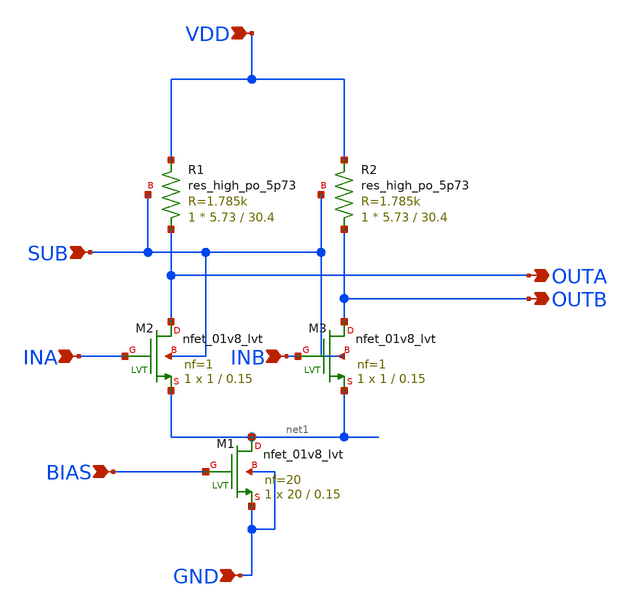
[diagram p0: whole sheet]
** sch_path: hiarachy_final/buffer_amp.sch
**.subckt buffer_amp INA INB BIAS GND VDD SUB OUTA OUTB
*.ipin INA
*.ipin INB
*.ipin BIAS
*.ipin GND
*.ipin VDD
*.ipin SUB
*.opin OUTA
*.opin OUTB
XM1 net1 BIAS GND GND sky130_fd_pr__nfet_01v8_lvt L=0.15 W=20 nf=20 ad='int((nf+1)/2) * W/nf * 0.29'
+ as='int((nf+2)/2) * W/nf * 0.29' pd='2*int((nf+1)/2) * (W/nf + 0.29)' ps='2*int((nf+2)/2) * (W/nf + 0.29)'
+ nrd='0.29 / W' nrs='0.29 / W' sa=0 sb=0 sd=0 mult=1 m=1
XM2 OUTA INA net1 SUB sky130_fd_pr__nfet_01v8_lvt L=0.15 W=1 nf=1 ad='int((nf+1)/2) * W/nf * 0.29' as='int((nf+2)/2) * W/nf * 0.29'
+ pd='2*int((nf+1)/2) * (W/nf + 0.29)' ps='2*int((nf+2)/2) * (W/nf + 0.29)' nrd='0.29 / W' nrs='0.29 / W'
+ sa=0 sb=0 sd=0 mult=1 m=1
XM3 OUTB INB net1 SUB sky130_fd_pr__nfet_01v8_lvt L=0.15 W=1 nf=1 ad='int((nf+1)/2) * W/nf * 0.29' as='int((nf+2)/2) * W/nf * 0.29'
+ pd='2*int((nf+1)/2) * (W/nf + 0.29)' ps='2*int((nf+2)/2) * (W/nf + 0.29)' nrd='0.29 / W' nrs='0.29 / W'
+ sa=0 sb=0 sd=0 mult=1 m=1
XR2 OUTB VDD SUB sky130_fd_pr__res_high_po_5p73 L=30.4 mult=1 m=1
XR1 OUTA VDD SUB sky130_fd_pr__res_high_po_5p73 L=30.4 mult=1 m=1
**.ends
.end
